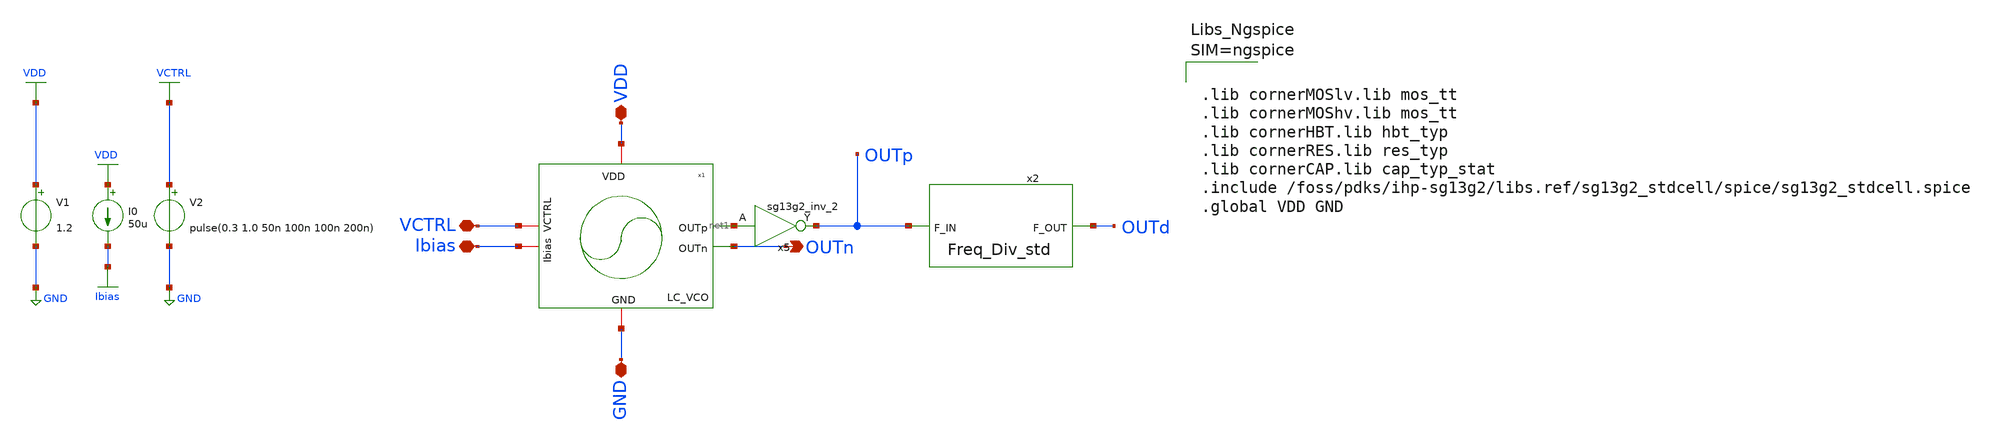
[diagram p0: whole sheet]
** sch_path: schematic/blocks/top-pll/LCVCO_temp_Fredivider_tb.sch
* IHP-GmbH/IHP-Open-PDK/ihp-sg13g2/libs.tech/xschem/sg13g2_stdcells/sg13g2_inv_2.sch:
* Copyright 2023 IHP PDK Authors
* Licensed under the Apache License, Version 2.0 (the "License");
**.subckt LCVCO_temp_Fredivider_tb OUTn VDD VCTRL GND Ibias
*.opin OUTn
*.iopin VDD
*.iopin VCTRL
*.iopin GND
*.iopin Ibias
V1 VDD GND 1.2
V2 VCTRL GND pulse(0.3 1.0 50n 100n 100n 200n)
I0 VDD Ibias 50u
x5 OUTp net1 VDD GND sg13g2_inv_2
x1 VDD net1 OUTn Ibias VCTRL GND LC_VCO
x2 OUTp OUTd Freq_Div_std
**** begin user architecture code



.lib cornerMOSlv.lib mos_tt
.lib cornerMOShv.lib mos_tt
.lib cornerHBT.lib hbt_typ
.lib cornerRES.lib res_typ
.lib cornerCAP.lib cap_typ_stat
.include /foss/pdks/ihp-sg13g2/libs.ref/sg13g2_stdcell/spice/sg13g2_stdcell.spice
.global VDD GND







.model freq_div freq_div
.include ./IHP_4nH_Inductor.spice
.param temp=27
.control
pre_osdi ./freq_div.osdi
save all
*.ic v(OUTp)=0.6

tran 1p 200n UIC

linearize v(OUTp) v(Vctrl) v(outd)

    let n_pts = length(time)
    let freq_vector = unitvec(n_pts) * 0

    * Advanced script to calculate instantaneous frequency
    let i = 1
    let last_cross = 0
    while i < length(time)
        if (v(OUTp)[i] >= 0.6) & (v(OUTp)[i-1] < 0.6)
            let current_cross = time[i]
            let period = current_cross - last_cross
            let inst_freq = 1 / period
            let freq_vector[i] = inst_freq
            let last_cross = current_cross
        else
            let freq_vector[i] = freq_vector[i-1]
        end
        let i = i + 1
    end

* Save transient waveform to raw file
write LCVCO_freqdiv.raw

*quit 0
.endc



**** end user architecture code
**.ends

* expanding   symbol:  sg13g2_stdcells/sg13g2_inv_2.sym # of pins=2
** sym_path: sg13g2_stdcells/sg13g2_inv_2.sym
** sch_path: sg13g2_stdcells/sg13g2_inv_2.sch
.subckt sg13g2_inv_2 Y A VDD VSS
*.opin Y
*.ipin A
*.iopin VDD
*.iopin VSS
XM1 Y A VSS VSS sg13_lv_nmos w=1.48u l=130.00n ng=2 m=1 mm_ok=1
XM2 Y A VDD VDD sg13_lv_pmos w=2.24u l=130.00n ng=2 m=1 mm_ok=1
.ends


* expanding   symbol:
*+  /foss/designs/iic_osic_tools/frac-n-pll-vco-unic_cass/schematic/blocks/lc-vco/LC_VCO.sym # of pins=6
** sym_path: /foss/designs/iic_osic_tools/frac-n-pll-vco-unic_cass/schematic/blocks/lc-vco/LC_VCO.sym
** sch_path: /foss/designs/iic_osic_tools/frac-n-pll-vco-unic_cass/schematic/blocks/lc-vco/LC_VCO.sch
.subckt LC_VCO VDD OUTp OUTn Ibias VCTRL GND
*.iopin VDD
*.opin OUTp
*.opin OUTn
*.iopin GND
*.iopin VCTRL
*.iopin Ibias
XM6 net1 Ibias GND GND sg13_lv_nmos w=1u l=0.15u ng=1 m=60 mm_ok=1
XM5 Ibias Ibias GND GND sg13_lv_nmos w=1u l=0.15u ng=1 m=1 mm_ok=1
XM4 OUTp OUTn VDD VDD sg13_lv_pmos w=8.5u l=0.5u ng=1 m=13 mm_ok=1
X5M3 OUTn OUTp VDD VDD sg13_lv_pmos w=8.5u l=0.5u ng=1 m=13 mm_ok=1
XM2 OUTp OUTn net1 GND sg13_lv_nmos w=2u l=0.5u ng=1 m=12 mm_ok=1
XM1 OUTn OUTp net1 GND sg13_lv_nmos w=2u l=0.5u ng=1 m=12 mm_ok=1
XC3 OUTp OUTn cap_cmim w=4.0e-6 l=4.0e-6 m=13.6 mm_ok=1
XMv2 OUTp VCTRL OUTp VDD sg13_lv_pmos w=4u l=4u ng=1 m=22 mm_ok=1
XMv1 OUTn VCTRL OUTn VDD sg13_lv_pmos w=4u l=4u ng=1 m=22 mm_ok=1
XR1 OUTp OUTn sub! rhigh w=1e-6 l=1e-6 m=1.23 b=0 mm_ok=1
x1 OUTn OUTp ihp_4nh_inductor
.ends


* expanding   symbol:
*+  /foss/designs/iic_osic_tools/frac-n-pll-vco-unic_cass/schematic/blocks/top-pll/FD/Freq_Div_std.sym # of pins=2
** sym_path: /foss/designs/iic_osic_tools/frac-n-pll-vco-unic_cass/schematic/blocks/top-pll/FD/Freq_Div_std.sym
** sch_path: /foss/designs/iic_osic_tools/frac-n-pll-vco-unic_cass/schematic/blocks/top-pll/FD/Freq_Div_std.sch
.subckt Freq_Div_std F_IN F_OUT
*.opin F_OUT
*.ipin F_IN
x6 net3 net1 F_IN net1 VDD VDD GND sg13g2_dfrbp_1
x5 net4 net2 net3 net2 VDD VDD GND sg13g2_dfrbp_2
x7 net6 net5 net4 net5 VDD VDD GND sg13g2_dfrbp_2
x8 F_OUT net7 net6 net7 VDD VDD GND sg13g2_dfrbp_2
.ends


* expanding   symbol:  sg13g2_stdcells/sg13g2_dfrbp_1.sym # of pins=5
** sym_path: sg13g2_stdcells/sg13g2_dfrbp_1.sym
** sch_path: sg13g2_stdcells/sg13g2_dfrbp_1.sch
.subckt sg13g2_dfrbp_1 Q Q_N CLK D RESET_B VDD VSS
*.ipin D
*.ipin RESET_B
*.ipin CLK
*.opin Q
*.opin Q_N
*.iopin VDD
*.iopin VSS
XM1 Db D net10 VSS sg13_lv_nmos w=420.00n l=130.00n ng=1 m=1 mm_ok=1
XM2 net10 RESET_B VSS VSS sg13_lv_nmos w=420.00n l=130.00n ng=1 m=1 mm_ok=1
XM3 net1 clkneg net9 VSS sg13_lv_nmos w=420.00n l=130.00n ng=1 m=1 mm_ok=1
XM4 net9 net1 VSS VSS sg13_lv_nmos w=420.00n l=130.00n ng=1 m=1 mm_ok=1
XM5 net1 net1 net5 VSS sg13_lv_nmos w=420.00n l=130.00n ng=1 m=1 mm_ok=1
XM6 net5 RESET_B VSS VSS sg13_lv_nmos w=420.00n l=130.00n ng=1 m=1 mm_ok=1
XM7 Q_N net1 VSS VSS sg13_lv_nmos w=740.00n l=130.00n ng=1 m=1 mm_ok=1
XM8 net2 net1 VSS VSS sg13_lv_nmos w=740.00n l=130.00n ng=1 m=1 mm_ok=1
XM9 Q net2 VSS VSS sg13_lv_nmos w=740.00n l=130.00n ng=1 m=1 mm_ok=1
XM10 clkneg CLK VSS VSS sg13_lv_nmos w=740.00n l=130.00n ng=1 m=1 mm_ok=1
XM11 clkpos clkneg VSS VSS sg13_lv_nmos w=740.00n l=130.00n ng=1 m=1 mm_ok=1
XM12 Db clkneg net3 VSS sg13_lv_nmos w=420.00n l=130.00n ng=1 m=1 mm_ok=1
XM13 net3 clkpos net8 VSS sg13_lv_nmos w=420.00n l=130.00n ng=1 m=1 mm_ok=1
XM14 net8 net3 net4 VSS sg13_lv_nmos w=420.00n l=130.00n ng=1 m=1 mm_ok=1
XM15 net4 RESET_B VSS VSS sg13_lv_nmos w=420.00n l=130.00n ng=1 m=1 mm_ok=1
XM16 net3 net3 VSS VSS sg13_lv_nmos w=740.00n l=130.00n ng=1 m=1 mm_ok=1
XM17 net3 clkpos net1 VSS sg13_lv_nmos w=740.00n l=130.00n ng=1 m=1 mm_ok=1
XM18 Db RESET_B VDD VDD sg13_lv_pmos w=420.00n l=130.00n ng=1 m=1 mm_ok=1
XM19 Db D VDD VDD sg13_lv_pmos w=420.00n l=130.00n ng=1 m=1 mm_ok=1
XM20 net7 net1 VDD VDD sg13_lv_pmos w=420.00n l=130.00n ng=1 m=1 mm_ok=1
XM21 net1 clkpos net7 VDD sg13_lv_pmos w=420.00n l=130.00n ng=1 m=1 mm_ok=1
XM22 net1 net1 VDD VDD sg13_lv_pmos w=420.00n l=130.00n ng=1 m=1 mm_ok=1
XM23 net1 RESET_B VDD VDD sg13_lv_pmos w=420.00n l=130.00n ng=1 m=1 mm_ok=1
XM24 Q_N net1 VDD VDD sg13_lv_pmos w=1.12u l=130.00n ng=1 m=1 mm_ok=1
XM25 net2 net1 VDD VDD sg13_lv_pmos w=1.12u l=130.00n ng=1 m=1 mm_ok=1
XM26 Q net2 VDD VDD sg13_lv_pmos w=1.12u l=130.00n ng=1 m=1 mm_ok=1
XM27 clkneg CLK VDD VDD sg13_lv_pmos w=1.12u l=130.00n ng=1 m=1 mm_ok=1
XM28 clkpos clkneg VDD VDD sg13_lv_pmos w=1.12u l=130.00n ng=1 m=1 mm_ok=1
XM29 Db clkpos net3 VDD sg13_lv_pmos w=420.00n l=130.00n ng=1 m=1 mm_ok=1
XM30 net6 net3 VDD VDD sg13_lv_pmos w=420.00n l=130.00n ng=1 m=1 mm_ok=1
XM31 net3 clkneg net6 VDD sg13_lv_pmos w=420.00n l=130.00n ng=1 m=1 mm_ok=1
XM32 net3 RESET_B VDD VDD sg13_lv_pmos w=420.00n l=130.00n ng=1 m=1 mm_ok=1
XM33 net3 net3 VDD VDD sg13_lv_pmos w=1.000u l=130.00n ng=1 m=1 mm_ok=1
XM34 net3 clkneg net1 VDD sg13_lv_pmos w=1.000u l=130.00n ng=1 m=1 mm_ok=1
.ends


* expanding   symbol:  sg13g2_stdcells/sg13g2_dfrbp_2.sym # of pins=5
** sym_path: sg13g2_stdcells/sg13g2_dfrbp_2.sym
** sch_path: sg13g2_stdcells/sg13g2_dfrbp_2.sch
.subckt sg13g2_dfrbp_2 Q Q_N CLK D RESET_B VDD VSS
*.ipin D
*.ipin RESET_B
*.ipin CLK
*.opin Q
*.opin Q_N
*.iopin VDD
*.iopin VSS
XM1 Db D net12 VSS sg13_lv_nmos w=420.00n l=130.00n ng=1 m=1 mm_ok=1
XM2 net12 RESET_B VSS VSS sg13_lv_nmos w=420.00n l=130.00n ng=1 m=1 mm_ok=1
XM3 net2 clkneg net11 VSS sg13_lv_nmos w=420.00n l=130.00n ng=1 m=1 mm_ok=1
XM4 net11 net3 VSS VSS sg13_lv_nmos w=420.00n l=130.00n ng=1 m=1 mm_ok=1
XM5 net3 net2 net7 VSS sg13_lv_nmos w=420.00n l=130.00n ng=1 m=1 mm_ok=1
XM6 net7 RESET_B VSS VSS sg13_lv_nmos w=420.00n l=130.00n ng=1 m=1 mm_ok=1
XM7 Q_N net2 VSS VSS sg13_lv_nmos w=1.48u l=130.00n ng=2 m=1 mm_ok=1
XM8 net1 net2 VSS VSS sg13_lv_nmos w=640.00n l=130.00n ng=1 m=1 mm_ok=1
XM9 Q net1 VSS VSS sg13_lv_nmos w=1.48u l=130.00n ng=2 m=1 mm_ok=1
XM10 clkneg CLK VSS VSS sg13_lv_nmos w=740.00n l=130.00n ng=1 m=1 mm_ok=1
XM11 clkpos clkneg VSS VSS sg13_lv_nmos w=740.00n l=130.00n ng=1 m=1 mm_ok=1
XM12 Db clkneg net4 VSS sg13_lv_nmos w=420.00n l=130.00n ng=1 m=1 mm_ok=1
XM13 net4 clkpos net10 VSS sg13_lv_nmos w=420.00n l=130.00n ng=1 m=1 mm_ok=1
XM14 net10 net5 net6 VSS sg13_lv_nmos w=420.00n l=130.00n ng=1 m=1 mm_ok=1
XM15 net6 RESET_B VSS VSS sg13_lv_nmos w=420.00n l=130.00n ng=1 m=1 mm_ok=1
XM16 net5 net4 VSS VSS sg13_lv_nmos w=740.00n l=130.00n ng=1 m=1 mm_ok=1
XM17 net5 clkpos net2 VSS sg13_lv_nmos w=740.00n l=130.00n ng=1 m=1 mm_ok=1
XM18 Db RESET_B VDD VDD sg13_lv_pmos w=420.00n l=130.00n ng=1 m=1 mm_ok=1
XM19 Db D VDD VDD sg13_lv_pmos w=420.00n l=130.00n ng=1 m=1 mm_ok=1
XM20 net9 net3 VDD VDD sg13_lv_pmos w=420.00n l=130.00n ng=1 m=1 mm_ok=1
XM21 net2 clkpos net9 VDD sg13_lv_pmos w=420.00n l=130.00n ng=1 m=1 mm_ok=1
XM22 net3 net2 VDD VDD sg13_lv_pmos w=420.00n l=130.00n ng=1 m=1 mm_ok=1
XM23 net3 RESET_B VDD VDD sg13_lv_pmos w=420.00n l=130.00n ng=1 m=1 mm_ok=1
XM24 Q_N net2 VDD VDD sg13_lv_pmos w=2.24u l=130.00n ng=2 m=1 mm_ok=1
XM25 net1 net2 VDD VDD sg13_lv_pmos w=1.000u l=130.00n ng=1 m=1 mm_ok=1
XM26 Q net1 VDD VDD sg13_lv_pmos w=2.24u l=130.00n ng=2 m=1 mm_ok=1
XM27 clkneg CLK VDD VDD sg13_lv_pmos w=1.12u l=130.00n ng=1 m=1 mm_ok=1
XM28 clkpos clkneg VDD VDD sg13_lv_pmos w=1.12u l=130.00n ng=1 m=1 mm_ok=1
XM29 Db clkpos net4 VDD sg13_lv_pmos w=420.00n l=130.00n ng=1 m=1 mm_ok=1
XM30 net8 net5 VDD VDD sg13_lv_pmos w=420.00n l=130.00n ng=1 m=1 mm_ok=1
XM31 net4 clkneg net8 VDD sg13_lv_pmos w=420.00n l=130.00n ng=1 m=1 mm_ok=1
XM32 net4 RESET_B VDD VDD sg13_lv_pmos w=420.00n l=130.00n ng=1 m=1 mm_ok=1
XM33 net5 net4 VDD VDD sg13_lv_pmos w=1.000u l=130.00n ng=1 m=1 mm_ok=1
XM34 net5 clkneg net2 VDD sg13_lv_pmos w=1.000u l=130.00n ng=1 m=1 mm_ok=1
.ends

.GLOBAL GND
.GLOBAL VDD
.GLOBAL VCTRL
.GLOBAL Ibias
.end
